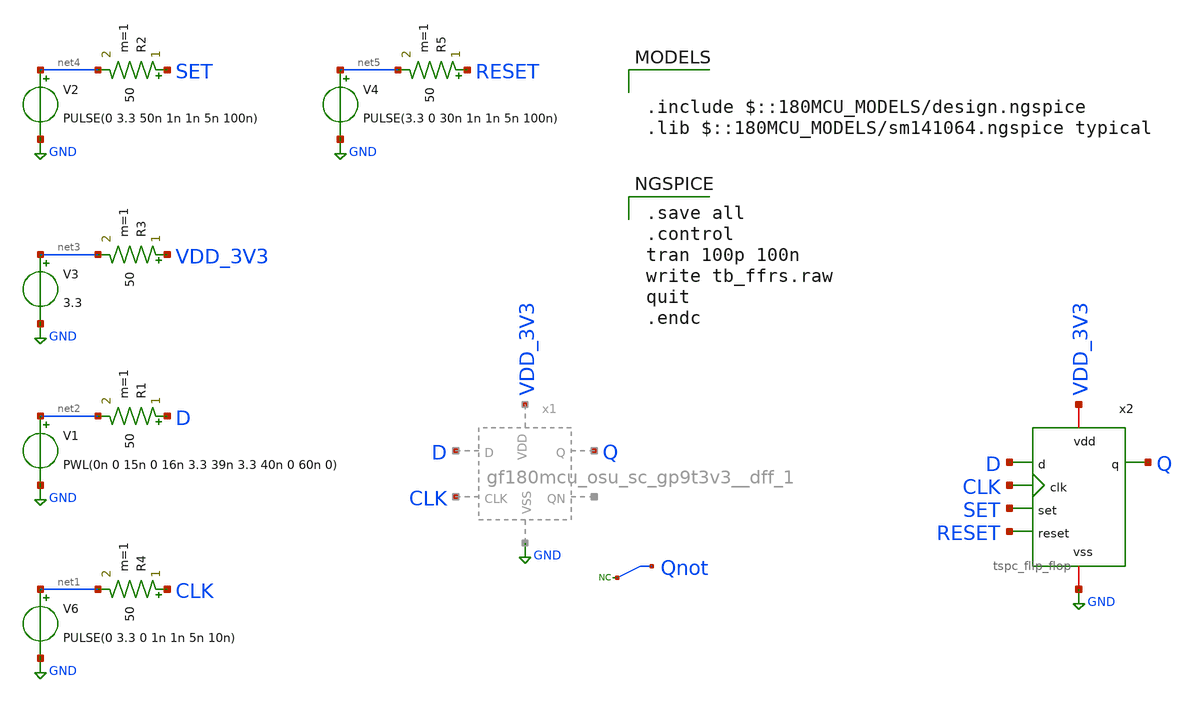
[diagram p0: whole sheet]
** sch_path: designs/libs/digital_cells/tb_ffrs.sch
**.subckt tb_ffrs
V6 net1 GND PULSE(0 3.3 0 1n 1n 5n 10n)
R4 CLK net1 50 m=1
V1 net2 GND PWL(0n 0 15n 0 16n 3.3 39n 3.3 40n 0 60n 0)
R1 D net2 50 m=1
V3 net3 GND 3.3
R3 VDD_3V3 net3 50 m=1
V2 net4 GND PULSE(0 3.3 50n 1n 1n 5n 100n)
R2 SET net4 50 m=1
V4 net5 GND PULSE(3.3 0 30n 1n 1n 5n 100n)
R5 RESET net5 50 m=1
x2 VDD_3V3 GND D CLK SET RESET Q tspc_flip_flop
* noconn Qnot
**** begin user architecture code

.include $::180MCU_MODELS/design.ngspice
.lib $::180MCU_MODELS/sm141064.ngspice typical


.save all
.control
tran 100p 100n
write tb_ffrs.raw
quit
.endc

**** end user architecture code
**.ends

* expanding   symbol:  libs/digital_cells/gf180mcu_osu_sc_gp9t3v3__dff_1.sym # of pins=6
** sym_path: designs/libs/digital_cells/gf180mcu_osu_sc_gp9t3v3__dff_1.sym
** sch_path: designs/libs/digital_cells/gf180mcu_osu_sc_gp9t3v3__dff_1.sch
.subckt gf180mcu_osu_sc_gp9t3v3__dff_1 CLK D Q VDD QN VSS
*.ipin D
*.ipin CLK
*.opin Q
*.opin QN
*.ipin VDD
*.ipin VSS
XM1 CLKb CLK VDD VDD pfet_03v3 L=0.3u W=1.7u nf=1 ad='int((nf+1)/2) * W/nf * 0.18u' as='int((nf+2)/2) * W/nf * 0.18u'
+ pd='2*int((nf+1)/2) * (W/nf + 0.18u)' ps='2*int((nf+2)/2) * (W/nf + 0.18u)' nrd='0.18u / W' nrs='0.18u / W'
+ sa=0 sb=0 sd=0 m=1
XM2 CLKb CLK VSS VSS nfet_03v3 L=0.3u W=0.85u nf=1 ad='int((nf+1)/2) * W/nf * 0.18u' as='int((nf+2)/2) * W/nf * 0.18u'
+ pd='2*int((nf+1)/2) * (W/nf + 0.18u)' ps='2*int((nf+2)/2) * (W/nf + 0.18u)' nrd='0.18u / W' nrs='0.18u / W'
+ sa=0 sb=0 sd=0 m=1
XM3 net1 CLK net2 VDD pfet_03v3 L=0.3u W=1.7u nf=1 ad='int((nf+1)/2) * W/nf * 0.18u' as='int((nf+2)/2) * W/nf * 0.18u'
+ pd='2*int((nf+1)/2) * (W/nf + 0.18u)' ps='2*int((nf+2)/2) * (W/nf + 0.18u)' nrd='0.18u / W' nrs='0.18u / W'
+ sa=0 sb=0 sd=0 m=1
XM4 net1 CLKb net3 VSS nfet_03v3 L=0.3u W=0.85u nf=1 ad='int((nf+1)/2) * W/nf * 0.18u' as='int((nf+2)/2) * W/nf * 0.18u'
+ pd='2*int((nf+1)/2) * (W/nf + 0.18u)' ps='2*int((nf+2)/2) * (W/nf + 0.18u)' nrd='0.18u / W' nrs='0.18u / W'
+ sa=0 sb=0 sd=0 m=1
XM5 net2 D VDD VDD pfet_03v3 L=0.3u W=1.7u nf=1 ad='int((nf+1)/2) * W/nf * 0.18u' as='int((nf+2)/2) * W/nf * 0.18u'
+ pd='2*int((nf+1)/2) * (W/nf + 0.18u)' ps='2*int((nf+2)/2) * (W/nf + 0.18u)' nrd='0.18u / W' nrs='0.18u / W'
+ sa=0 sb=0 sd=0 m=1
XM6 net3 D VSS VSS nfet_03v3 L=0.3u W=0.85u nf=1 ad='int((nf+1)/2) * W/nf * 0.18u' as='int((nf+2)/2) * W/nf * 0.18u'
+ pd='2*int((nf+1)/2) * (W/nf + 0.18u)' ps='2*int((nf+2)/2) * (W/nf + 0.18u)' nrd='0.18u / W' nrs='0.18u / W'
+ sa=0 sb=0 sd=0 m=1
XM7 net1 CLK net4 VDD pfet_03v3 L=0.3u W=1.7u nf=1 ad='int((nf+1)/2) * W/nf * 0.18u' as='int((nf+2)/2) * W/nf * 0.18u'
+ pd='2*int((nf+1)/2) * (W/nf + 0.18u)' ps='2*int((nf+2)/2) * (W/nf + 0.18u)' nrd='0.18u / W' nrs='0.18u / W'
+ sa=0 sb=0 sd=0 m=1
XM8 net1 CLKb net5 VSS nfet_03v3 L=0.3u W=0.60u nf=1 ad='int((nf+1)/2) * W/nf * 0.18u' as='int((nf+2)/2) * W/nf * 0.18u'
+ pd='2*int((nf+1)/2) * (W/nf + 0.18u)' ps='2*int((nf+2)/2) * (W/nf + 0.18u)' nrd='0.18u / W' nrs='0.18u / W'
+ sa=0 sb=0 sd=0 m=1
XM9 net4 net6 VDD VDD pfet_03v3 L=0.3u W=1.7u nf=1 ad='int((nf+1)/2) * W/nf * 0.18u' as='int((nf+2)/2) * W/nf * 0.18u'
+ pd='2*int((nf+1)/2) * (W/nf + 0.18u)' ps='2*int((nf+2)/2) * (W/nf + 0.18u)' nrd='0.18u / W' nrs='0.18u / W'
+ sa=0 sb=0 sd=0 m=1
XM10 net5 net6 VSS VSS nfet_03v3 L=0.3u W=0.60u nf=1 ad='int((nf+1)/2) * W/nf * 0.18u' as='int((nf+2)/2) * W/nf * 0.18u'
+ pd='2*int((nf+1)/2) * (W/nf + 0.18u)' ps='2*int((nf+2)/2) * (W/nf + 0.18u)' nrd='0.18u / W' nrs='0.18u / W'
+ sa=0 sb=0 sd=0 m=1
XM11 net6 net1 VDD VDD pfet_03v3 L=0.3u W=1.7u nf=1 ad='int((nf+1)/2) * W/nf * 0.18u' as='int((nf+2)/2) * W/nf * 0.18u'
+ pd='2*int((nf+1)/2) * (W/nf + 0.18u)' ps='2*int((nf+2)/2) * (W/nf + 0.18u)' nrd='0.18u / W' nrs='0.18u / W'
+ sa=0 sb=0 sd=0 m=1
XM12 net6 net1 VSS VSS nfet_03v3 L=0.3u W=0.85u nf=1 ad='int((nf+1)/2) * W/nf * 0.18u' as='int((nf+2)/2) * W/nf * 0.18u'
+ pd='2*int((nf+1)/2) * (W/nf + 0.18u)' ps='2*int((nf+2)/2) * (W/nf + 0.18u)' nrd='0.18u / W' nrs='0.18u / W'
+ sa=0 sb=0 sd=0 m=1
XM13 net7 CLKb net8 VDD pfet_03v3 L=0.3u W=1.7u nf=1 ad='int((nf+1)/2) * W/nf * 0.18u' as='int((nf+2)/2) * W/nf * 0.18u'
+ pd='2*int((nf+1)/2) * (W/nf + 0.18u)' ps='2*int((nf+2)/2) * (W/nf + 0.18u)' nrd='0.18u / W' nrs='0.18u / W'
+ sa=0 sb=0 sd=0 m=1
XM14 net7 CLK net9 VSS nfet_03v3 L=0.3u W=0.85u nf=1 ad='int((nf+1)/2) * W/nf * 0.18u' as='int((nf+2)/2) * W/nf * 0.18u'
+ pd='2*int((nf+1)/2) * (W/nf + 0.18u)' ps='2*int((nf+2)/2) * (W/nf + 0.18u)' nrd='0.18u / W' nrs='0.18u / W'
+ sa=0 sb=0 sd=0 m=1
XM15 net8 net6 VDD VDD pfet_03v3 L=0.3u W=1.7u nf=1 ad='int((nf+1)/2) * W/nf * 0.18u' as='int((nf+2)/2) * W/nf * 0.18u'
+ pd='2*int((nf+1)/2) * (W/nf + 0.18u)' ps='2*int((nf+2)/2) * (W/nf + 0.18u)' nrd='0.18u / W' nrs='0.18u / W'
+ sa=0 sb=0 sd=0 m=1
XM16 net9 net6 VSS VSS nfet_03v3 L=0.3u W=0.85u nf=1 ad='int((nf+1)/2) * W/nf * 0.18u' as='int((nf+2)/2) * W/nf * 0.18u'
+ pd='2*int((nf+1)/2) * (W/nf + 0.18u)' ps='2*int((nf+2)/2) * (W/nf + 0.18u)' nrd='0.18u / W' nrs='0.18u / W'
+ sa=0 sb=0 sd=0 m=1
XM17 net7 CLKb net10 VDD pfet_03v3 L=0.3u W=1.7u nf=1 ad='int((nf+1)/2) * W/nf * 0.18u' as='int((nf+2)/2) * W/nf * 0.18u'
+ pd='2*int((nf+1)/2) * (W/nf + 0.18u)' ps='2*int((nf+2)/2) * (W/nf + 0.18u)' nrd='0.18u / W' nrs='0.18u / W'
+ sa=0 sb=0 sd=0 m=1
XM18 net7 CLK net11 VSS nfet_03v3 L=0.3u W=0.60u nf=1 ad='int((nf+1)/2) * W/nf * 0.18u' as='int((nf+2)/2) * W/nf * 0.18u'
+ pd='2*int((nf+1)/2) * (W/nf + 0.18u)' ps='2*int((nf+2)/2) * (W/nf + 0.18u)' nrd='0.18u / W' nrs='0.18u / W'
+ sa=0 sb=0 sd=0 m=1
XM19 net10 net12 VDD VDD pfet_03v3 L=0.3u W=1.7u nf=1 ad='int((nf+1)/2) * W/nf * 0.18u' as='int((nf+2)/2) * W/nf * 0.18u'
+ pd='2*int((nf+1)/2) * (W/nf + 0.18u)' ps='2*int((nf+2)/2) * (W/nf + 0.18u)' nrd='0.18u / W' nrs='0.18u / W'
+ sa=0 sb=0 sd=0 m=1
XM20 net11 net12 VSS VSS nfet_03v3 L=0.3u W=0.60u nf=1 ad='int((nf+1)/2) * W/nf * 0.18u' as='int((nf+2)/2) * W/nf * 0.18u'
+ pd='2*int((nf+1)/2) * (W/nf + 0.18u)' ps='2*int((nf+2)/2) * (W/nf + 0.18u)' nrd='0.18u / W' nrs='0.18u / W'
+ sa=0 sb=0 sd=0 m=1
XM21 net12 net7 VDD VDD pfet_03v3 L=0.3u W=1.7u nf=1 ad='int((nf+1)/2) * W/nf * 0.18u' as='int((nf+2)/2) * W/nf * 0.18u'
+ pd='2*int((nf+1)/2) * (W/nf + 0.18u)' ps='2*int((nf+2)/2) * (W/nf + 0.18u)' nrd='0.18u / W' nrs='0.18u / W'
+ sa=0 sb=0 sd=0 m=2
XM22 net12 net7 VSS VSS nfet_03v3 L=0.3u W=0.85u nf=1 ad='int((nf+1)/2) * W/nf * 0.18u' as='int((nf+2)/2) * W/nf * 0.18u'
+ pd='2*int((nf+1)/2) * (W/nf + 0.18u)' ps='2*int((nf+2)/2) * (W/nf + 0.18u)' nrd='0.18u / W' nrs='0.18u / W'
+ sa=0 sb=0 sd=0 m=2
XM23 QN net12 VDD VDD pfet_03v3 L=0.3u W=1.7u nf=1 ad='int((nf+1)/2) * W/nf * 0.18u' as='int((nf+2)/2) * W/nf * 0.18u'
+ pd='2*int((nf+1)/2) * (W/nf + 0.18u)' ps='2*int((nf+2)/2) * (W/nf + 0.18u)' nrd='0.18u / W' nrs='0.18u / W'
+ sa=0 sb=0 sd=0 m=1
XM24 QN net12 VSS VSS nfet_03v3 L=0.3u W=0.85u nf=1 ad='int((nf+1)/2) * W/nf * 0.18u' as='int((nf+2)/2) * W/nf * 0.18u'
+ pd='2*int((nf+1)/2) * (W/nf + 0.18u)' ps='2*int((nf+2)/2) * (W/nf + 0.18u)' nrd='0.18u / W' nrs='0.18u / W'
+ sa=0 sb=0 sd=0 m=1
XM25 Q QN VDD VDD pfet_03v3 L=0.3u W=1.7u nf=1 ad='int((nf+1)/2) * W/nf * 0.18u' as='int((nf+2)/2) * W/nf * 0.18u'
+ pd='2*int((nf+1)/2) * (W/nf + 0.18u)' ps='2*int((nf+2)/2) * (W/nf + 0.18u)' nrd='0.18u / W' nrs='0.18u / W'
+ sa=0 sb=0 sd=0 m=1
XM26 Q QN VSS VSS nfet_03v3 L=0.3u W=0.85u nf=1 ad='int((nf+1)/2) * W/nf * 0.18u' as='int((nf+2)/2) * W/nf * 0.18u'
+ pd='2*int((nf+1)/2) * (W/nf + 0.18u)' ps='2*int((nf+2)/2) * (W/nf + 0.18u)' nrd='0.18u / W' nrs='0.18u / W'
+ sa=0 sb=0 sd=0 m=1
.ends


* expanding   symbol:  libs/tspc_flip_flop/tspc_flip_flop.sym # of pins=7
** sym_path: designs/libs/tspc_flip_flop/tspc_flip_flop.sym
** sch_path: designs/libs/tspc_flip_flop/tspc_flip_flop.sch
.subckt tspc_flip_flop vdd vss d clk set reset q
*.iopin vdd
*.iopin vss
*.ipin d
*.ipin clk
*.ipin set
*.ipin reset
*.opin q
XM1 b1 d vss vss nfet_03v3 L=0.28u W=1u nf=1 ad='int((nf+1)/2) * W/nf * 0.18u' as='int((nf+2)/2) * W/nf * 0.18u'
+ pd='2*int((nf+1)/2) * (W/nf + 0.18u)' ps='2*int((nf+2)/2) * (W/nf + 0.18u)' nrd='0.18u / W' nrs='0.18u / W'
+ sa=0 sb=0 sd=0 m=1
XM2 b1 clk net1 net1 pfet_03v3 L=0.28u W=4u nf=1 ad='int((nf+1)/2) * W/nf * 0.18u' as='int((nf+2)/2) * W/nf * 0.18u'
+ pd='2*int((nf+1)/2) * (W/nf + 0.18u)' ps='2*int((nf+2)/2) * (W/nf + 0.18u)' nrd='0.18u / W' nrs='0.18u / W'
+ sa=0 sb=0 sd=0 m=1
XM3 net1 d vdd vdd pfet_03v3 L=0.28u W=4u nf=1 ad='int((nf+1)/2) * W/nf * 0.18u' as='int((nf+2)/2) * W/nf * 0.18u'
+ pd='2*int((nf+1)/2) * (W/nf + 0.18u)' ps='2*int((nf+2)/2) * (W/nf + 0.18u)' nrd='0.18u / W' nrs='0.18u / W'
+ sa=0 sb=0 sd=0 m=1
XM4 b2 clk vdd vdd pfet_03v3 L=0.28u W=20u nf=1 ad='int((nf+1)/2) * W/nf * 0.18u' as='int((nf+2)/2) * W/nf * 0.18u'
+ pd='2*int((nf+1)/2) * (W/nf + 0.18u)' ps='2*int((nf+2)/2) * (W/nf + 0.18u)' nrd='0.18u / W' nrs='0.18u / W'
+ sa=0 sb=0 sd=0 m=1
XM5 b2 b1 net2 vss nfet_03v3 L=0.28u W=20u nf=1 ad='int((nf+1)/2) * W/nf * 0.18u' as='int((nf+2)/2) * W/nf * 0.18u'
+ pd='2*int((nf+1)/2) * (W/nf + 0.18u)' ps='2*int((nf+2)/2) * (W/nf + 0.18u)' nrd='0.18u / W' nrs='0.18u / W'
+ sa=0 sb=0 sd=0 m=1
XM6 net2 clk vss vss nfet_03v3 L=0.28u W=20u nf=1 ad='int((nf+1)/2) * W/nf * 0.18u' as='int((nf+2)/2) * W/nf * 0.18u'
+ pd='2*int((nf+1)/2) * (W/nf + 0.18u)' ps='2*int((nf+2)/2) * (W/nf + 0.18u)' nrd='0.18u / W' nrs='0.18u / W'
+ sa=0 sb=0 sd=0 m=1
XM7 net4 b2 vss vss nfet_03v3 L=0.28u W=80u nf=1 ad='int((nf+1)/2) * W/nf * 0.18u' as='int((nf+2)/2) * W/nf * 0.18u'
+ pd='2*int((nf+1)/2) * (W/nf + 0.18u)' ps='2*int((nf+2)/2) * (W/nf + 0.18u)' nrd='0.18u / W' nrs='0.18u / W'
+ sa=0 sb=0 sd=0 m=1
XM8 b3 clk net4 vss nfet_03v3 L=0.28u W=80u nf=1 ad='int((nf+1)/2) * W/nf * 0.18u' as='int((nf+2)/2) * W/nf * 0.18u'
+ pd='2*int((nf+1)/2) * (W/nf + 0.18u)' ps='2*int((nf+2)/2) * (W/nf + 0.18u)' nrd='0.18u / W' nrs='0.18u / W'
+ sa=0 sb=0 sd=0 m=1
XM9 b3 set net3 net3 pfet_03v3 L=0.28u W=80u nf=1 ad='int((nf+1)/2) * W/nf * 0.18u' as='int((nf+2)/2) * W/nf * 0.18u'
+ pd='2*int((nf+1)/2) * (W/nf + 0.18u)' ps='2*int((nf+2)/2) * (W/nf + 0.18u)' nrd='0.18u / W' nrs='0.18u / W'
+ sa=0 sb=0 sd=0 m=1
XM10 net3 b2 vdd vdd pfet_03v3 L=0.28u W=80u nf=1 ad='int((nf+1)/2) * W/nf * 0.18u' as='int((nf+2)/2) * W/nf * 0.18u'
+ pd='2*int((nf+1)/2) * (W/nf + 0.18u)' ps='2*int((nf+2)/2) * (W/nf + 0.18u)' nrd='0.18u / W' nrs='0.18u / W'
+ sa=0 sb=0 sd=0 m=1
XM11 b3 reset vdd vdd pfet_03v3 L=0.28u W=0.22u nf=1 ad='int((nf+1)/2) * W/nf * 0.18u' as='int((nf+2)/2) * W/nf * 0.18u'
+ pd='2*int((nf+1)/2) * (W/nf + 0.18u)' ps='2*int((nf+2)/2) * (W/nf + 0.18u)' nrd='0.18u / W' nrs='0.18u / W'
+ sa=0 sb=0 sd=0 m=1
XM12 b3 set vss vss nfet_03v3 L=0.28u W=0.22u nf=1 ad='int((nf+1)/2) * W/nf * 0.18u' as='int((nf+2)/2) * W/nf * 0.18u'
+ pd='2*int((nf+1)/2) * (W/nf + 0.18u)' ps='2*int((nf+2)/2) * (W/nf + 0.18u)' nrd='0.18u / W' nrs='0.18u / W'
+ sa=0 sb=0 sd=0 m=1
XM13 q b3 vdd vdd pfet_03v3 L=0.28u W=0.22u nf=1 ad='int((nf+1)/2) * W/nf * 0.18u' as='int((nf+2)/2) * W/nf * 0.18u'
+ pd='2*int((nf+1)/2) * (W/nf + 0.18u)' ps='2*int((nf+2)/2) * (W/nf + 0.18u)' nrd='0.18u / W' nrs='0.18u / W'
+ sa=0 sb=0 sd=0 m=1
XM14 q b3 vss vss nfet_03v3 L=0.28u W=0.22u nf=1 ad='int((nf+1)/2) * W/nf * 0.18u' as='int((nf+2)/2) * W/nf * 0.18u'
+ pd='2*int((nf+1)/2) * (W/nf + 0.18u)' ps='2*int((nf+2)/2) * (W/nf + 0.18u)' nrd='0.18u / W' nrs='0.18u / W'
+ sa=0 sb=0 sd=0 m=1
.ends

.GLOBAL GND
.GLOBAL VDD
.GLOBAL VSS
.end
